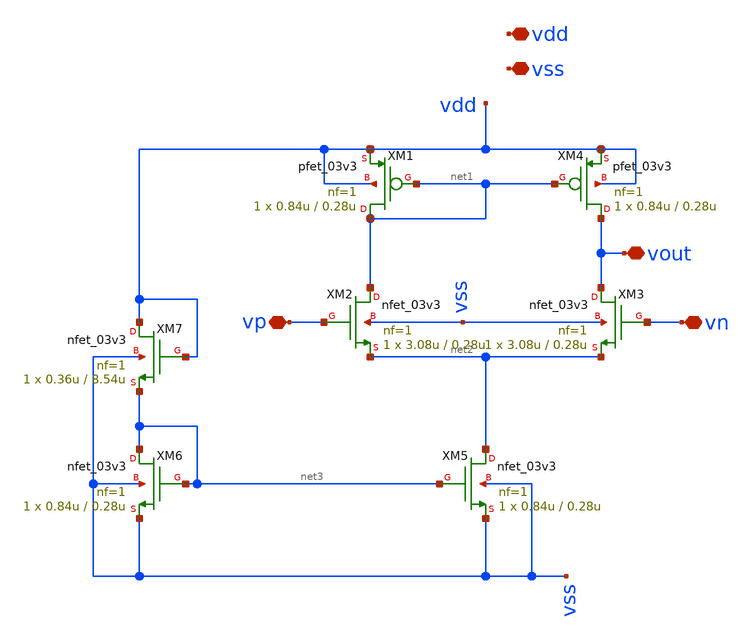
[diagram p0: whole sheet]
** sch_path: designs/libs/core_LIF_comp/core_ota_1stage/ota_1stage.sch
**.subckt ota_1stage vdd vss vp vn vout
*.iopin vdd
*.iopin vss
*.iopin vp
*.iopin vn
*.iopin vout
XM1 net1 net1 vdd vdd pfet_03v3 L=0.28u W=0.84u nf=1 ad='int((nf+1)/2) * W/nf * 0.18u' as='int((nf+2)/2) * W/nf * 0.18u'
+ pd='2*int((nf+1)/2) * (W/nf + 0.18u)' ps='2*int((nf+2)/2) * (W/nf + 0.18u)' nrd='0.18u / W' nrs='0.18u / W'
+ sa=0 sb=0 sd=0 m=1
XM2 net1 vp net2 vss nfet_03v3 L=0.28u W=3.08u nf=1 ad='int((nf+1)/2) * W/nf * 0.18u' as='int((nf+2)/2) * W/nf * 0.18u'
+ pd='2*int((nf+1)/2) * (W/nf + 0.18u)' ps='2*int((nf+2)/2) * (W/nf + 0.18u)' nrd='0.18u / W' nrs='0.18u / W'
+ sa=0 sb=0 sd=0 m=1
XM4 vout net1 vdd vdd pfet_03v3 L=0.28u W=0.84u nf=1 ad='int((nf+1)/2) * W/nf * 0.18u' as='int((nf+2)/2) * W/nf * 0.18u'
+ pd='2*int((nf+1)/2) * (W/nf + 0.18u)' ps='2*int((nf+2)/2) * (W/nf + 0.18u)' nrd='0.18u / W' nrs='0.18u / W'
+ sa=0 sb=0 sd=0 m=1
XM3 vout vn net2 vss nfet_03v3 L=0.28u W=3.08u nf=1 ad='int((nf+1)/2) * W/nf * 0.18u' as='int((nf+2)/2) * W/nf * 0.18u'
+ pd='2*int((nf+1)/2) * (W/nf + 0.18u)' ps='2*int((nf+2)/2) * (W/nf + 0.18u)' nrd='0.18u / W' nrs='0.18u / W'
+ sa=0 sb=0 sd=0 m=1
XM5 net2 net3 vss vss nfet_03v3 L=0.28u W=0.84u nf=1 ad='int((nf+1)/2) * W/nf * 0.18u' as='int((nf+2)/2) * W/nf * 0.18u'
+ pd='2*int((nf+1)/2) * (W/nf + 0.18u)' ps='2*int((nf+2)/2) * (W/nf + 0.18u)' nrd='0.18u / W' nrs='0.18u / W'
+ sa=0 sb=0 sd=0 m=1
XM6 net3 net3 vss vss nfet_03v3 L=0.28u W=0.84u nf=1 ad='int((nf+1)/2) * W/nf * 0.18u' as='int((nf+2)/2) * W/nf * 0.18u'
+ pd='2*int((nf+1)/2) * (W/nf + 0.18u)' ps='2*int((nf+2)/2) * (W/nf + 0.18u)' nrd='0.18u / W' nrs='0.18u / W'
+ sa=0 sb=0 sd=0 m=1
XM7 vdd vdd net3 vss nfet_03v3 L=8.54u W=0.36u nf=1 ad='int((nf+1)/2) * W/nf * 0.18u' as='int((nf+2)/2) * W/nf * 0.18u'
+ pd='2*int((nf+1)/2) * (W/nf + 0.18u)' ps='2*int((nf+2)/2) * (W/nf + 0.18u)' nrd='0.18u / W' nrs='0.18u / W'
+ sa=0 sb=0 sd=0 m=1
**.ends
.end
